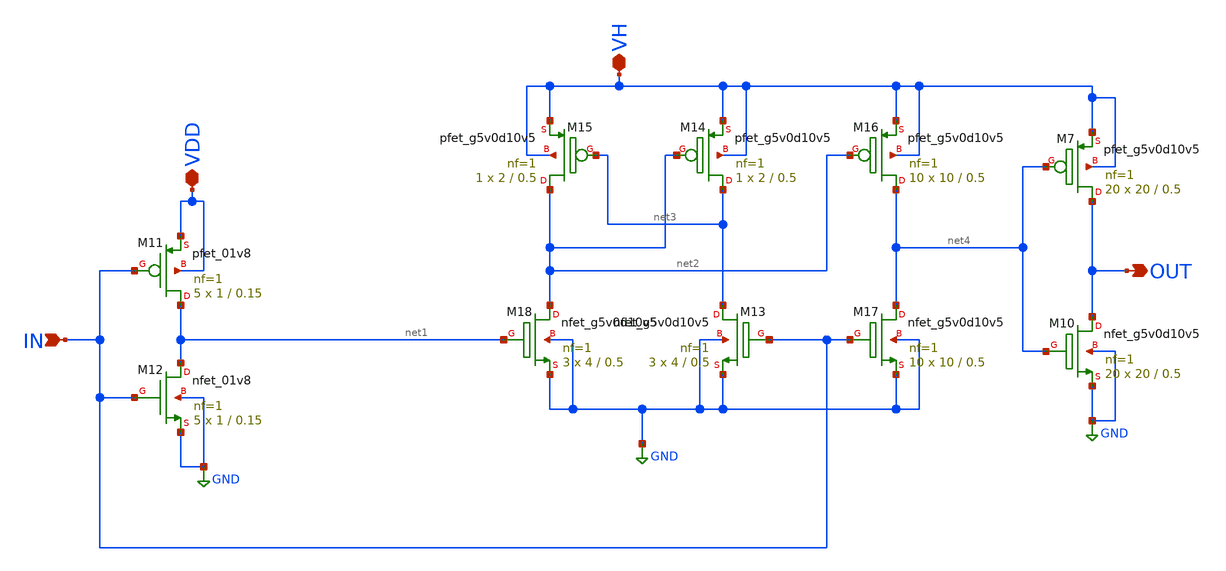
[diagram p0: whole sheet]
** sch_path: xschem/hierarchy_sch/LS_FINAL.sch
**.subckt LS_FINAL IN VDD VH OUT
*.ipin IN
*.iopin VDD
*.iopin VH
*.opin OUT
XM11 net1 IN VDD VDD sky130_fd_pr__pfet_01v8 L=0.15 W=1 nf=1 ad='int((nf+1)/2) * W/nf * 0.29' as='int((nf+2)/2) * W/nf * 0.29'
+ pd='2*int((nf+1)/2) * (W/nf + 0.29)' ps='2*int((nf+2)/2) * (W/nf + 0.29)' nrd='0.29 / W' nrs='0.29 / W'
+ sa=0 sb=0 sd=0 mult=5 m=5
XM12 net1 IN GND GND sky130_fd_pr__nfet_01v8 L=0.15 W=1 nf=1 ad='int((nf+1)/2) * W/nf * 0.29' as='int((nf+2)/2) * W/nf * 0.29'
+ pd='2*int((nf+1)/2) * (W/nf + 0.29)' ps='2*int((nf+2)/2) * (W/nf + 0.29)' nrd='0.29 / W' nrs='0.29 / W'
+ sa=0 sb=0 sd=0 mult=5 m=5
XM15 net2 net3 VH VH sky130_fd_pr__pfet_g5v0d10v5 L=0.5 W=2 nf=1 ad='int((nf+1)/2) * W/nf * 0.29' as='int((nf+2)/2) * W/nf * 0.29'
+ pd='2*int((nf+1)/2) * (W/nf + 0.29)' ps='2*int((nf+2)/2) * (W/nf + 0.29)' nrd='0.29 / W' nrs='0.29 / W'
+ sa=0 sb=0 sd=0 mult=1 m=1
XM14 net3 net2 VH VH sky130_fd_pr__pfet_g5v0d10v5 L=0.5 W=2 nf=1 ad='int((nf+1)/2) * W/nf * 0.29' as='int((nf+2)/2) * W/nf * 0.29'
+ pd='2*int((nf+1)/2) * (W/nf + 0.29)' ps='2*int((nf+2)/2) * (W/nf + 0.29)' nrd='0.29 / W' nrs='0.29 / W'
+ sa=0 sb=0 sd=0 mult=1 m=1
XM16 net4 net2 VH VH sky130_fd_pr__pfet_g5v0d10v5 L=0.5 W=10 nf=1 ad='int((nf+1)/2) * W/nf * 0.29' as='int((nf+2)/2) * W/nf * 0.29'
+ pd='2*int((nf+1)/2) * (W/nf + 0.29)' ps='2*int((nf+2)/2) * (W/nf + 0.29)' nrd='0.29 / W' nrs='0.29 / W'
+ sa=0 sb=0 sd=0 mult=10 m=10
XM18 net2 net1 GND GND sky130_fd_pr__nfet_g5v0d10v5 L=0.5 W=4 nf=1 ad='int((nf+1)/2) * W/nf * 0.29' as='int((nf+2)/2) * W/nf * 0.29'
+ pd='2*int((nf+1)/2) * (W/nf + 0.29)' ps='2*int((nf+2)/2) * (W/nf + 0.29)' nrd='0.29 / W' nrs='0.29 / W'
+ sa=0 sb=0 sd=0 mult=3 m=3
XM13 net3 IN GND GND sky130_fd_pr__nfet_g5v0d10v5 L=0.5 W=4 nf=1 ad='int((nf+1)/2) * W/nf * 0.29' as='int((nf+2)/2) * W/nf * 0.29'
+ pd='2*int((nf+1)/2) * (W/nf + 0.29)' ps='2*int((nf+2)/2) * (W/nf + 0.29)' nrd='0.29 / W' nrs='0.29 / W'
+ sa=0 sb=0 sd=0 mult=3 m=3
XM17 net4 IN GND GND sky130_fd_pr__nfet_g5v0d10v5 L=0.5 W=10 nf=1 ad='int((nf+1)/2) * W/nf * 0.29' as='int((nf+2)/2) * W/nf * 0.29'
+ pd='2*int((nf+1)/2) * (W/nf + 0.29)' ps='2*int((nf+2)/2) * (W/nf + 0.29)' nrd='0.29 / W' nrs='0.29 / W'
+ sa=0 sb=0 sd=0 mult=10 m=10
XM7 OUT net4 VH VH sky130_fd_pr__pfet_g5v0d10v5 L=0.5 W=20 nf=1 ad='int((nf+1)/2) * W/nf * 0.29' as='int((nf+2)/2) * W/nf * 0.29'
+ pd='2*int((nf+1)/2) * (W/nf + 0.29)' ps='2*int((nf+2)/2) * (W/nf + 0.29)' nrd='0.29 / W' nrs='0.29 / W'
+ sa=0 sb=0 sd=0 mult=20 m=20
XM10 OUT net4 GND GND sky130_fd_pr__nfet_g5v0d10v5 L=0.5 W=20 nf=1 ad='int((nf+1)/2) * W/nf * 0.29' as='int((nf+2)/2) * W/nf * 0.29'
+ pd='2*int((nf+1)/2) * (W/nf + 0.29)' ps='2*int((nf+2)/2) * (W/nf + 0.29)' nrd='0.29 / W' nrs='0.29 / W'
+ sa=0 sb=0 sd=0 mult=20 m=20
**.ends
.GLOBAL GND
.end
